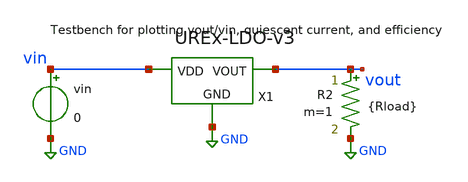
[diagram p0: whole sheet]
** sch_path: xschem/testbenches/VoutvsVin-v3.sch
**.subckt VoutvsVin-v3
vin vin GND 0
R2 vout GND {Rload} m=1
X1 vin vout GND UREx-LDO-v3
**** begin user architecture code



.lib /usr/local/share/pdk/sky130A/libs.tech/ngspice/sky130.lib.spice tt
.param Rload = 20
.dc vin 0.5 5 0.1
*.tran 5u 10m

.control
run
let Rload = 20
let iout = vout/Rload
let iq = (-i(vin))-iout
let eff = (iout*vout*100)/((iout+iq)*vin)

plot v(vout)
plot iq
plot eff

.endc


**** end user architecture code
**.ends

* expanding   symbol:  UREx-LDO-v3.sym # of pins=3
** sym_path: xschem/UREx-LDO-v3.sym
** sch_path: xschem/UREx-LDO-v3.sch
.subckt UREx-LDO-v3 VDD VOUT GND
*.ipin VDD
*.opin VOUT
*.ipin GND
C2 net2 gate 6p m=1
I1 VDD net4 4u
V3 v- GND 0.6
XM1 net3 v- net1 GND sky130_fd_pr__nfet_01v8_lvt L=1 W=0.8 nf=1 ad='int((1 + 1)/2) * 0.8 / 1 * 0.29'
+ as='int((1 + 2)/2) * 0.8 / 1 * 0.29' pd='2*int((1 + 1)/2) * (0.8 / 1 + 0.29)' ps='2*int((1 + 2)/2) * (0.8 / 1 + 0.29)'
+ nrd='0.29 / 0.8 ' nrs='0.29 / 0.8 ' sa=0 sb=0 sd=0 mult=1 m=1
XM4 net2 net3 VDD VDD sky130_fd_pr__pfet_01v8_lvt L=1 W=0.5 nf=1 ad='int((1 + 1)/2) * 0.5 / 1 * 0.29'
+ as='int((1 + 2)/2) * 0.5 / 1 * 0.29' pd='2*int((1 + 1)/2) * (0.5 / 1 + 0.29)' ps='2*int((1 + 2)/2) * (0.5 / 1 + 0.29)'
+ nrd='0.29 / 0.5 ' nrs='0.29 / 0.5 ' sa=0 sb=0 sd=0 mult=1 m=1
XM3 net3 net3 VDD VDD sky130_fd_pr__pfet_01v8_lvt L=1 W=0.5 nf=1 ad='int((1 + 1)/2) * 0.5 / 1 * 0.29'
+ as='int((1 + 2)/2) * 0.5 / 1 * 0.29' pd='2*int((1 + 1)/2) * (0.5 / 1 + 0.29)' ps='2*int((1 + 2)/2) * (0.5 / 1 + 0.29)'
+ nrd='0.29 / 0.5 ' nrs='0.29 / 0.5 ' sa=0 sb=0 sd=0 mult=1 m=1
XM2 net2 v+ net1 GND sky130_fd_pr__nfet_01v8_lvt L=1 W=0.8 nf=1 ad='int((1 + 1)/2) * 0.8 / 1 * 0.29'
+ as='int((1 + 2)/2) * 0.8 / 1 * 0.29' pd='2*int((1 + 1)/2) * (0.8 / 1 + 0.29)' ps='2*int((1 + 2)/2) * (0.8 / 1 + 0.29)'
+ nrd='0.29 / 0.8 ' nrs='0.29 / 0.8 ' sa=0 sb=0 sd=0 mult=1 m=1
XM8 net4 net4 GND GND sky130_fd_pr__nfet_01v8_lvt L=1 W=1.2 nf=1 ad='int((1 + 1)/2) * 1.2 / 1 * 0.29'
+ as='int((1 + 2)/2) * 1.2 / 1 * 0.29' pd='2*int((1 + 1)/2) * (1.2 / 1 + 0.29)' ps='2*int((1 + 2)/2) * (1.2 / 1 + 0.29)'
+ nrd='0.29 / 1.2 ' nrs='0.29 / 1.2 ' sa=0 sb=0 sd=0 mult=1 m=1
XM5 net1 net4 GND GND sky130_fd_pr__nfet_01v8_lvt L=1 W=1.2 nf=1 ad='int((1 + 1)/2) * 1.2 / 1 * 0.29'
+ as='int((1 + 2)/2) * 1.2 / 1 * 0.29' pd='2*int((1 + 1)/2) * (1.2 / 1 + 0.29)' ps='2*int((1 + 2)/2) * (1.2 / 1 + 0.29)'
+ nrd='0.29 / 1.2 ' nrs='0.29 / 1.2 ' sa=0 sb=0 sd=0 mult=1 m=1
XM7 gate net4 GND GND sky130_fd_pr__nfet_01v8_lvt L=0.15 W=3.1 nf=1 ad='int((1 + 1)/2) * 3.1 / 1 * 0.29'
+ as='int((1 + 2)/2) * 3.1 / 1 * 0.29' pd='2*int((1 + 1)/2) * (3.1 / 1 + 0.29)' ps='2*int((1 + 2)/2) * (3.1 / 1 + 0.29)'
+ nrd='0.29 / 3.1 ' nrs='0.29 / 3.1 ' sa=0 sb=0 sd=0 mult=1 m=1
XM6 gate net2 VDD VDD sky130_fd_pr__pfet_01v8_lvt L=0.35 W=4.2 nf=1 ad='int((1 + 1)/2) * 4.2 / 1 * 0.29'
+ as='int((1 + 2)/2) * 4.2 / 1 * 0.29' pd='2*int((1 + 1)/2) * (4.2 / 1 + 0.29)' ps='2*int((1 + 2)/2) * (4.2 / 1 + 0.29)'
+ nrd='0.29 / 4.2 ' nrs='0.29 / 4.2 ' sa=0 sb=0 sd=0 mult=1 m=1
R3 VOUT v+ 40k m=1
R4 v+ GND 60k m=1
XM9 VOUT gate VDD VDD sky130_fd_pr__pfet_01v8_lvt L=0.35 W=35 nf=1 ad='int((1 + 1)/2) * 35 / 1 * 0.29'
+ as='int((1 + 2)/2) * 35 / 1 * 0.29' pd='2*int((1 + 1)/2) * (35 / 1 + 0.29)' ps='2*int((1 + 2)/2) * (35 / 1 + 0.29)'
+ nrd='0.29 / 35 ' nrs='0.29 / 35 ' sa=0 sb=0 sd=0 mult=408 m=408
.ends

.GLOBAL GND
.end
